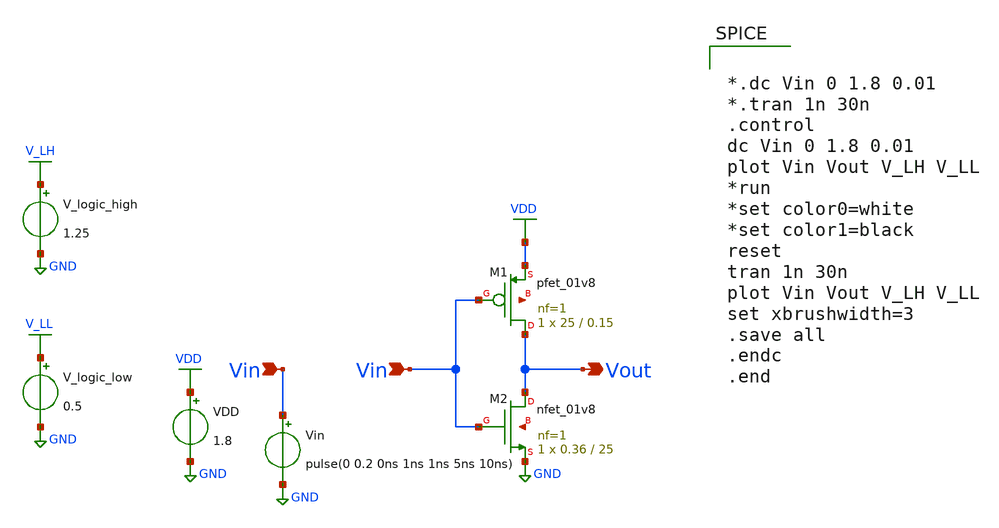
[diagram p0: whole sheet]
** sch_path: xschem/Vth_sch/test_ngspice/test_script.sch
**.subckt test_script Vin Vin Vout
*.ipin Vin
*.ipin Vin
*.opin Vout
VDD VDD GND 1.8
Vin Vin GND pulse(0 0.2 0ns 1ns 1ns 5ns 10ns)
XM1 Vout Vin VDD net1 sky130_fd_pr__pfet_01v8 L=0.15 W=25 nf=1 ad='int((nf+1)/2) * W/nf * 0.29' as='int((nf+2)/2) * W/nf * 0.29'
+ pd='2*int((nf+1)/2) * (W/nf + 0.29)' ps='2*int((nf+2)/2) * (W/nf + 0.29)' nrd='0.29 / W' nrs='0.29 / W'
+ sa=0 sb=0 sd=0 mult=1 m=1
XM2 Vout Vin GND net2 sky130_fd_pr__nfet_01v8 L=25 W=0.36 nf=1 ad='int((nf+1)/2) * W/nf * 0.29' as='int((nf+2)/2) * W/nf * 0.29'
+ pd='2*int((nf+1)/2) * (W/nf + 0.29)' ps='2*int((nf+2)/2) * (W/nf + 0.29)' nrd='0.29 / W' nrs='0.29 / W'
+ sa=0 sb=0 sd=0 mult=1 m=1
V_logic_high V_LH GND 1.25
V_logic_low V_LL GND 0.5
**** begin user architecture code


.lib /usr/local/share/pdk/sky130A/libs.tech/ngspice/sky130.lib.spice tt

.save all





*.dc Vin 0 1.8 0.01
*.tran 1n 30n
.control
dc Vin 0 1.8 0.01
plot Vin Vout V_LH V_LL
*run
*set color0=white
*set color1=black
reset
tran 1n 30n
plot Vin Vout V_LH V_LL
set xbrushwidth=3
.save all
.endc
.end


**** end user architecture code
**.ends
.GLOBAL VDD
.GLOBAL GND
.GLOBAL V_LH
.GLOBAL V_LL
.end
